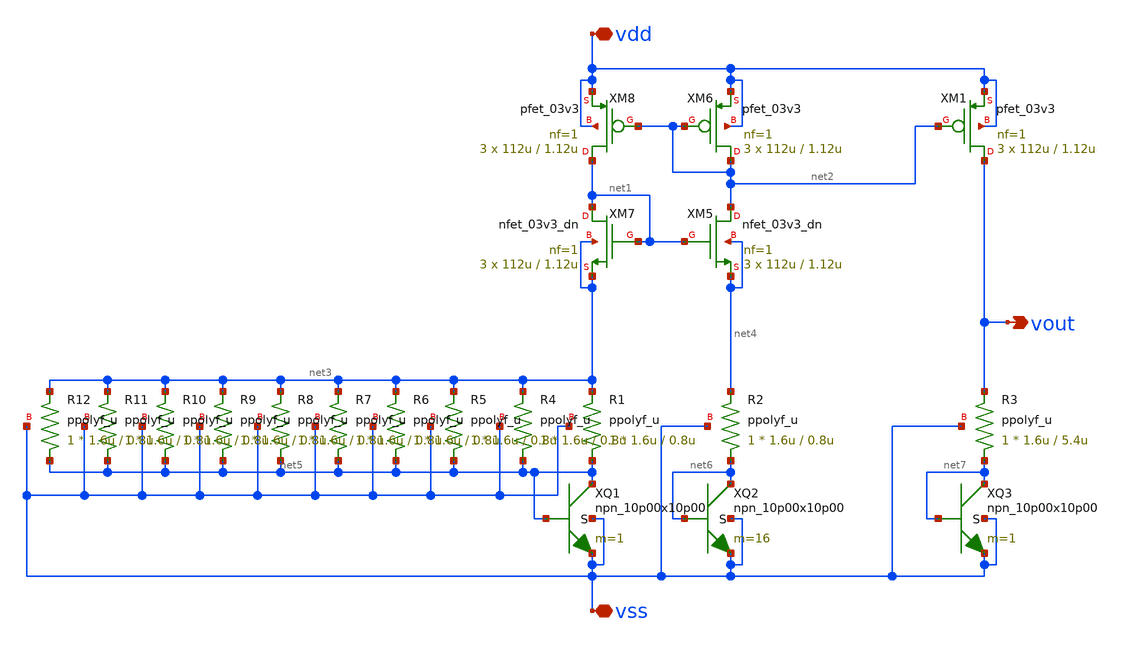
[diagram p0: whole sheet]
** sch_path: submit_version/xschem/bgr_diode_lvs.sch
**.subckt bgr_diode_lvs vdd vss vout
*.iopin vdd
*.iopin vss
*.opin vout
XM5 net2 net1 net4 net4 nfet_03v3_dn L=1.12u W=112u nf=1 ad='int((nf+1)/2) * W/nf * 0.18u' as='int((nf+2)/2) * W/nf * 0.18u'
+ pd='2*int((nf+1)/2) * (W/nf + 0.18u)' ps='2*int((nf+2)/2) * (W/nf + 0.18u)' nrd='0.18u / W' nrs='0.18u / W'
+ sa=0 sb=0 sd=0 m=3
XM6 net2 net2 vdd vdd pfet_03v3 L=1.12u W=112u nf=1 ad='int((nf+1)/2) * W/nf * 0.18u' as='int((nf+2)/2) * W/nf * 0.18u'
+ pd='2*int((nf+1)/2) * (W/nf + 0.18u)' ps='2*int((nf+2)/2) * (W/nf + 0.18u)' nrd='0.18u / W' nrs='0.18u / W'
+ sa=0 sb=0 sd=0 m=3
XM7 net1 net1 net3 net3 nfet_03v3_dn L=1.12u W=112u nf=1 ad='int((nf+1)/2) * W/nf * 0.18u' as='int((nf+2)/2) * W/nf * 0.18u'
+ pd='2*int((nf+1)/2) * (W/nf + 0.18u)' ps='2*int((nf+2)/2) * (W/nf + 0.18u)' nrd='0.18u / W' nrs='0.18u / W'
+ sa=0 sb=0 sd=0 m=3
XM8 net1 net2 vdd vdd pfet_03v3 L=1.12u W=112u nf=1 ad='int((nf+1)/2) * W/nf * 0.18u' as='int((nf+2)/2) * W/nf * 0.18u'
+ pd='2*int((nf+1)/2) * (W/nf + 0.18u)' ps='2*int((nf+2)/2) * (W/nf + 0.18u)' nrd='0.18u / W' nrs='0.18u / W'
+ sa=0 sb=0 sd=0 m=3
XQ1 net5 net5 vss vss npn_10p00x10p00 m=1
XQ2 net6 net6 vss vss npn_10p00x10p00 m=16
XM1 vout net2 vdd vdd pfet_03v3 L=1.12u W=112u nf=1 ad='int((nf+1)/2) * W/nf * 0.18u' as='int((nf+2)/2) * W/nf * 0.18u'
+ pd='2*int((nf+1)/2) * (W/nf + 0.18u)' ps='2*int((nf+2)/2) * (W/nf + 0.18u)' nrd='0.18u / W' nrs='0.18u / W'
+ sa=0 sb=0 sd=0 m=3
XQ3 net7 net7 vss vss npn_10p00x10p00 m=1
R1 net5 net3 vss ppolyf_u W=1.6u L=0.8u m=1
R2 net6 net4 vss ppolyf_u W=1.6u L=0.8u m=1
R3 net7 vout vss ppolyf_u W=1.6u L=5.4u m=1
R4 net5 net3 vss ppolyf_u W=1.6u L=0.8u m=1
R5 net5 net3 vss ppolyf_u W=1.6u L=0.8u m=1
R6 net5 net3 vss ppolyf_u W=1.6u L=0.8u m=1
R7 net5 net3 vss ppolyf_u W=1.6u L=0.8u m=1
R8 net5 net3 vss ppolyf_u W=1.6u L=0.8u m=1
R9 net5 net3 vss ppolyf_u W=1.6u L=0.8u m=1
R10 net5 net3 vss ppolyf_u W=1.6u L=0.8u m=1
R11 net5 net3 vss ppolyf_u W=1.6u L=0.8u m=1
R12 net5 net3 vss ppolyf_u W=1.6u L=0.8u m=1
**.ends
.end
